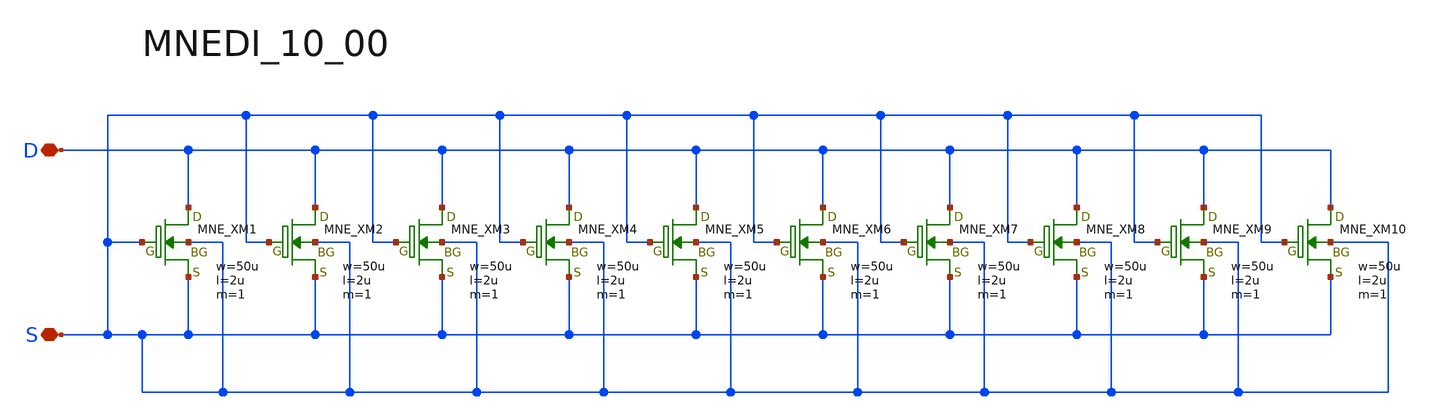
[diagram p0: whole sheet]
** sch_path: openIP62_rev1.0/IP62/Technology/tech/symbols/Xschem/IP62_2_ESD/MNEDI_10_00.sch
**.subckt MNEDI_10_00 D S
*.iopin D
*.iopin S
XM1 D S S S MNE w=50u l=2u as=0 ad=0 ps=0 pd=0 nrd=0 nrs=0 m=1
XM2 D S S S MNE w=50u l=2u as=0 ad=0 ps=0 pd=0 nrd=0 nrs=0 m=1
XM3 D S S S MNE w=50u l=2u as=0 ad=0 ps=0 pd=0 nrd=0 nrs=0 m=1
XM4 D S S S MNE w=50u l=2u as=0 ad=0 ps=0 pd=0 nrd=0 nrs=0 m=1
XM5 D S S S MNE w=50u l=2u as=0 ad=0 ps=0 pd=0 nrd=0 nrs=0 m=1
XM6 D S S S MNE w=50u l=2u as=0 ad=0 ps=0 pd=0 nrd=0 nrs=0 m=1
XM7 D S S S MNE w=50u l=2u as=0 ad=0 ps=0 pd=0 nrd=0 nrs=0 m=1
XM8 D S S S MNE w=50u l=2u as=0 ad=0 ps=0 pd=0 nrd=0 nrs=0 m=1
XM9 D S S S MNE w=50u l=2u as=0 ad=0 ps=0 pd=0 nrd=0 nrs=0 m=1
XM10 D S S S MNE w=50u l=2u as=0 ad=0 ps=0 pd=0 nrd=0 nrs=0 m=1
**.ends
.end
